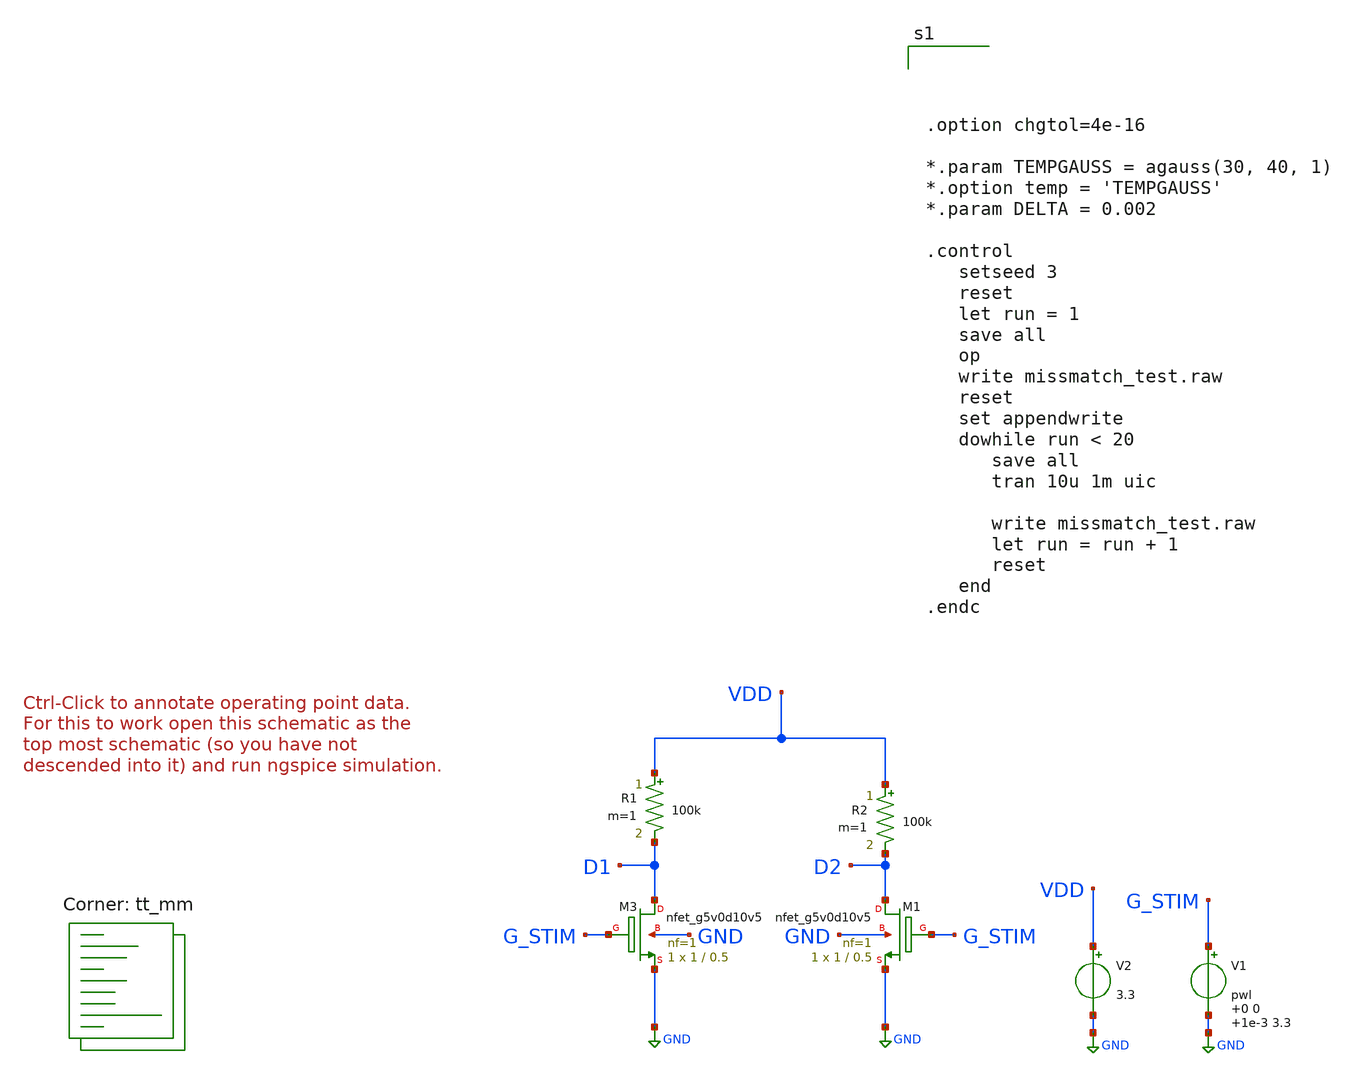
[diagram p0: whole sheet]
** sch_path: xschem/missmatch_test.sch
**.subckt missmatch_test
V1 G_STIM GND pwl 0 0 1e-3 3.3
V2 VDD GND 3.3
R1 VDD D1 100k m=1
R2 VDD D2 100k m=1
XM3 D1 G_STIM GND GND sky130_fd_pr__nfet_g5v0d10v5 L=0.5 W=1 nf=1 ad='int((nf+1)/2) * W/nf * 0.29' as='int((nf+2)/2) * W/nf * 0.29'
+ pd='2*int((nf+1)/2) * (W/nf + 0.29)' ps='2*int((nf+2)/2) * (W/nf + 0.29)' nrd='0.29 / W' nrs='0.29 / W'
+ sa=0 sb=0 sd=0 mult=1 m=1
XM1 D2 G_STIM GND GND sky130_fd_pr__nfet_g5v0d10v5 L=0.5 W=1 nf=1 ad='int((nf+1)/2) * W/nf * 0.29' as='int((nf+2)/2) * W/nf * 0.29'
+ pd='2*int((nf+1)/2) * (W/nf + 0.29)' ps='2*int((nf+2)/2) * (W/nf + 0.29)' nrd='0.29 / W' nrs='0.29 / W'
+ sa=0 sb=0 sd=0 mult=1 m=1
**** begin user architecture code
.lib $::SKYWATER_MODELS/sky130.lib.spice tt_mm




.option chgtol=4e-16

*.param TEMPGAUSS = agauss(30, 40, 1)
*.option temp = 'TEMPGAUSS'
*.param DELTA = 0.002

.control
   setseed 3
   reset
   let run = 1
   save all
   op
   write missmatch_test.raw
   reset
   set appendwrite
   dowhile run < 20
      save all
      tran 10u 1m uic

      write missmatch_test.raw
      let run = run + 1
      reset
   end
.endc


**** end user architecture code
**.ends
.GLOBAL GND
.end
